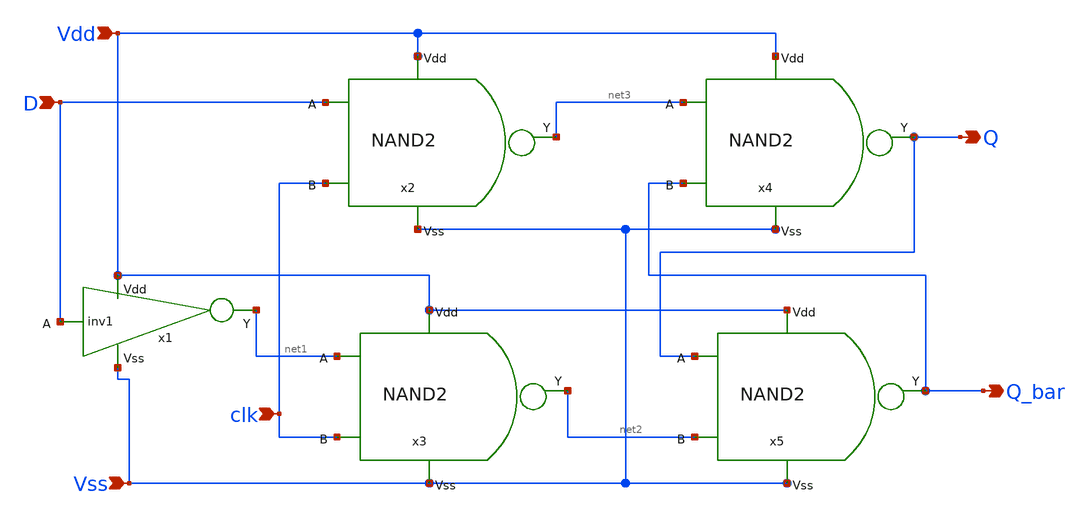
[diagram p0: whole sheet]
** sch_path: designs/D_ff1.sch
**.subckt D_ff1 D Vdd Vss clk Q Q_bar
*.ipin D
*.ipin Vdd
*.ipin Vss
*.ipin clk
*.opin Q
*.opin Q_bar
x1 Vdd D net1 Vss inv1
x2 Vdd net3 D clk Vss NAND2
x3 Vdd net2 net1 clk Vss NAND2
x4 Vdd Q net3 Q_bar Vss NAND2
x5 Vdd Q_bar Q net2 Vss NAND2
**.ends
.end
